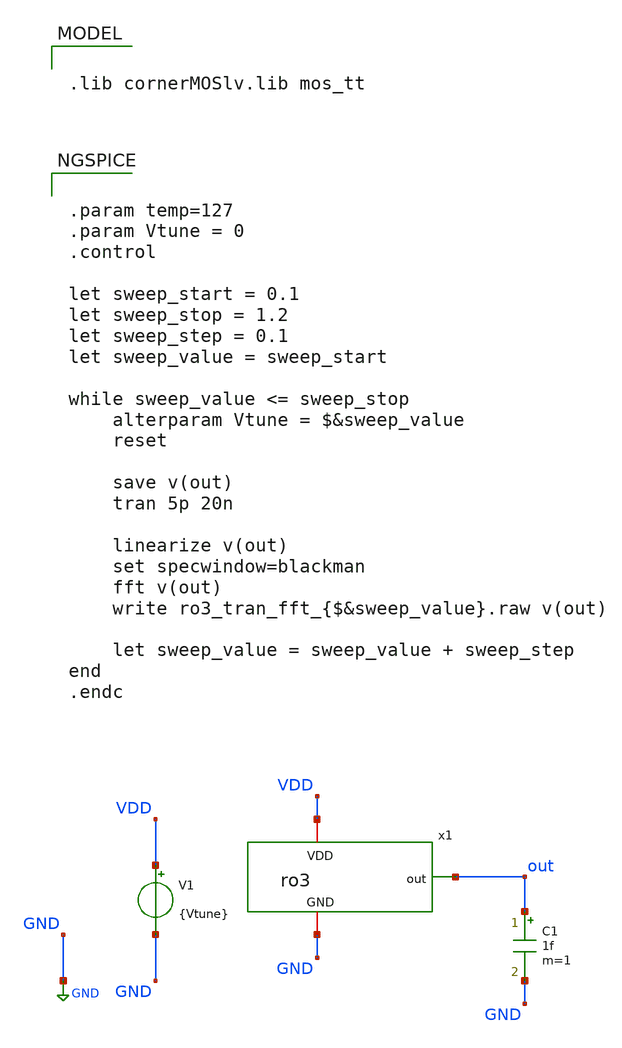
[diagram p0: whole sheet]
** sch_path: 20260719_tunnable_ring_oscillator/ro3_tb.sch
**.subckt ro3_tb
x1 out VDD GND ro3
V1 VDD GND {Vtune}
C1 out GND 1f m=1
**** begin user architecture code

.lib cornerMOSlv.lib mos_tt



.param temp=127
.param Vtune = 0
.control

let sweep_start = 0.1
let sweep_stop = 1.2
let sweep_step = 0.1
let sweep_value = sweep_start

while sweep_value <= sweep_stop
	alterparam Vtune = $&sweep_value
	reset

	save v(out)
	tran 5p 20n

	linearize v(out)
	set specwindow=blackman
	fft v(out)
	write ro3_tran_fft_{$&sweep_value}.raw v(out)

	let sweep_value = sweep_value + sweep_step
end
.endc


**** end user architecture code
**.ends

* expanding   symbol:  ro3.sym # of pins=3
** sym_path: 20260719_tunnable_ring_oscillator/ro3.sym
** sch_path: 20260719_tunnable_ring_oscillator/ro3.sch
.subckt ro3 out VDD GND
*.opin out
*.iopin VDD
*.iopin GND
XM1 net1 net2 GND GND sg13_lv_nmos w=0.15u l=0.13u ng=1 m=1 mm_ok=1
XM2 net1 net2 VDD VDD sg13_lv_pmos w=0.3u l=0.13u ng=1 m=1 mm_ok=1
XM3 net3 net1 GND GND sg13_lv_nmos w=0.15u l=0.13u ng=1 m=1 mm_ok=1
XM4 net3 net1 VDD VDD sg13_lv_pmos w=0.3u l=0.13u ng=1 m=1 mm_ok=1
XM5 net2 net3 GND GND sg13_lv_nmos w=0.15u l=0.13u ng=1 m=1 mm_ok=1
XM6 net2 net3 VDD VDD sg13_lv_pmos w=0.3u l=0.13u ng=1 m=1 mm_ok=1
XM7 out net2 GND GND sg13_lv_nmos w=0.15u l=0.13u ng=1 m=1 mm_ok=1
XM8 out net2 VDD VDD sg13_lv_pmos w=0.3u l=0.13u ng=1 m=1 mm_ok=1
.ends

.GLOBAL GND
.end
